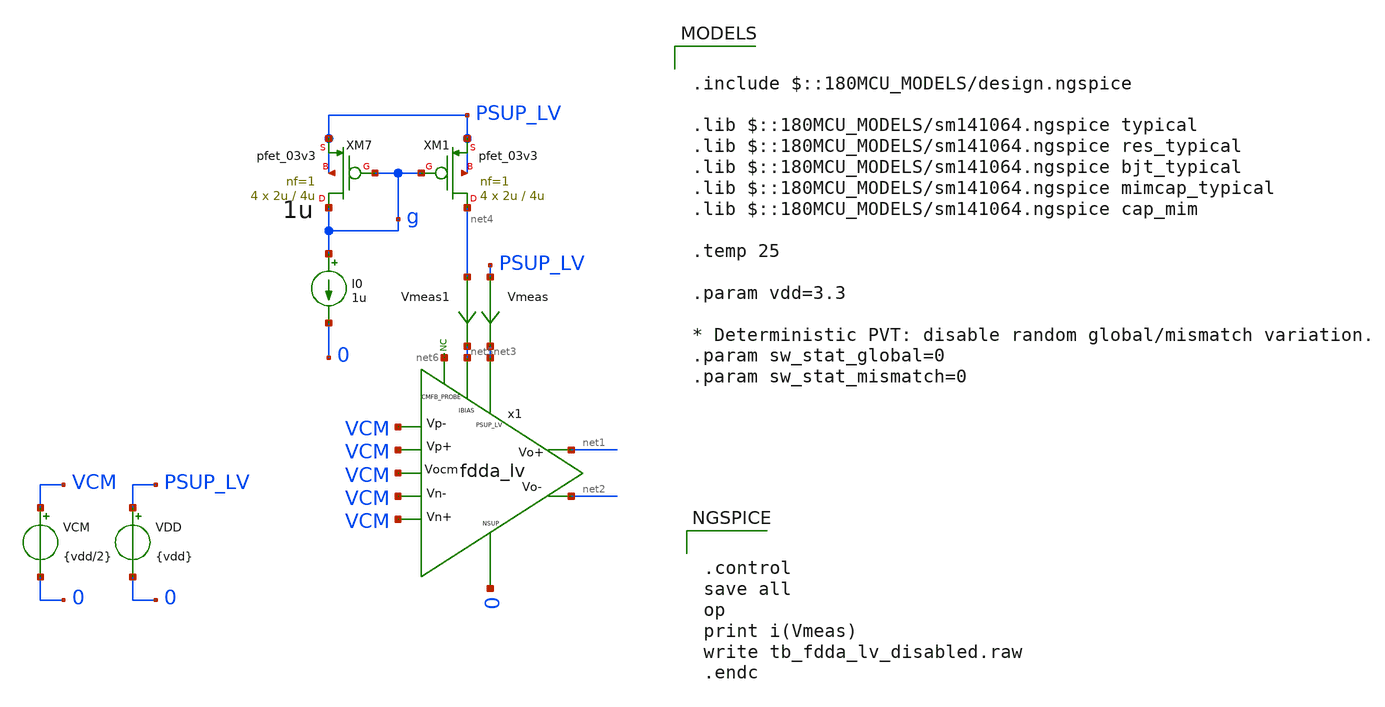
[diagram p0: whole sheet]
** sch_path: xschem/blocks/fdda_lv/tb_fdda_lv_disabled.sch
**.subckt tb_fdda_lv_disabled
x1 net3 VCM VCM VCM VCM net1 net2 net5 0 net6 VCM fdda_lv
* noconn #net6
VDD PSUP_LV 0 {vdd}
VCM VCM 0 {vdd/2}
Vmeas PSUP_LV net3 0
.save i(vmeas)
XM7 g g PSUP_LV PSUP_LV pfet_03v3 L=4u W=2u nf=1 ad='int((nf+1)/2) * W/nf * 0.18u' as='int((nf+2)/2) * W/nf * 0.18u'
+ pd='2*int((nf+1)/2) * (W/nf + 0.18u)' ps='2*int((nf+2)/2) * (W/nf + 0.18u)' nrd='0.18u / W' nrs='0.18u / W'
+ sa=0 sb=0 sd=0 m=4
XM1 net4 g PSUP_LV PSUP_LV pfet_03v3 L=4u W=2u nf=1 ad='int((nf+1)/2) * W/nf * 0.18u' as='int((nf+2)/2) * W/nf * 0.18u'
+ pd='2*int((nf+1)/2) * (W/nf + 0.18u)' ps='2*int((nf+2)/2) * (W/nf + 0.18u)' nrd='0.18u / W' nrs='0.18u / W'
+ sa=0 sb=0 sd=0 m=4
I0 g 0 1u
Vmeas1 net4 net5 0
.save i(vmeas1)
**** begin user architecture code


.control
save all
op
print i(Vmeas)
write tb_fdda_lv_disabled.raw
.endc



.include $::180MCU_MODELS/design.ngspice

.lib $::180MCU_MODELS/sm141064.ngspice typical
.lib $::180MCU_MODELS/sm141064.ngspice res_typical
.lib $::180MCU_MODELS/sm141064.ngspice bjt_typical
.lib $::180MCU_MODELS/sm141064.ngspice mimcap_typical
.lib $::180MCU_MODELS/sm141064.ngspice cap_mim

.temp 25

.param vdd=3.3

* Deterministic PVT: disable random global/mismatch variation.
.param sw_stat_global=0
.param sw_stat_mismatch=0


**** end user architecture code
**.ends
.end
